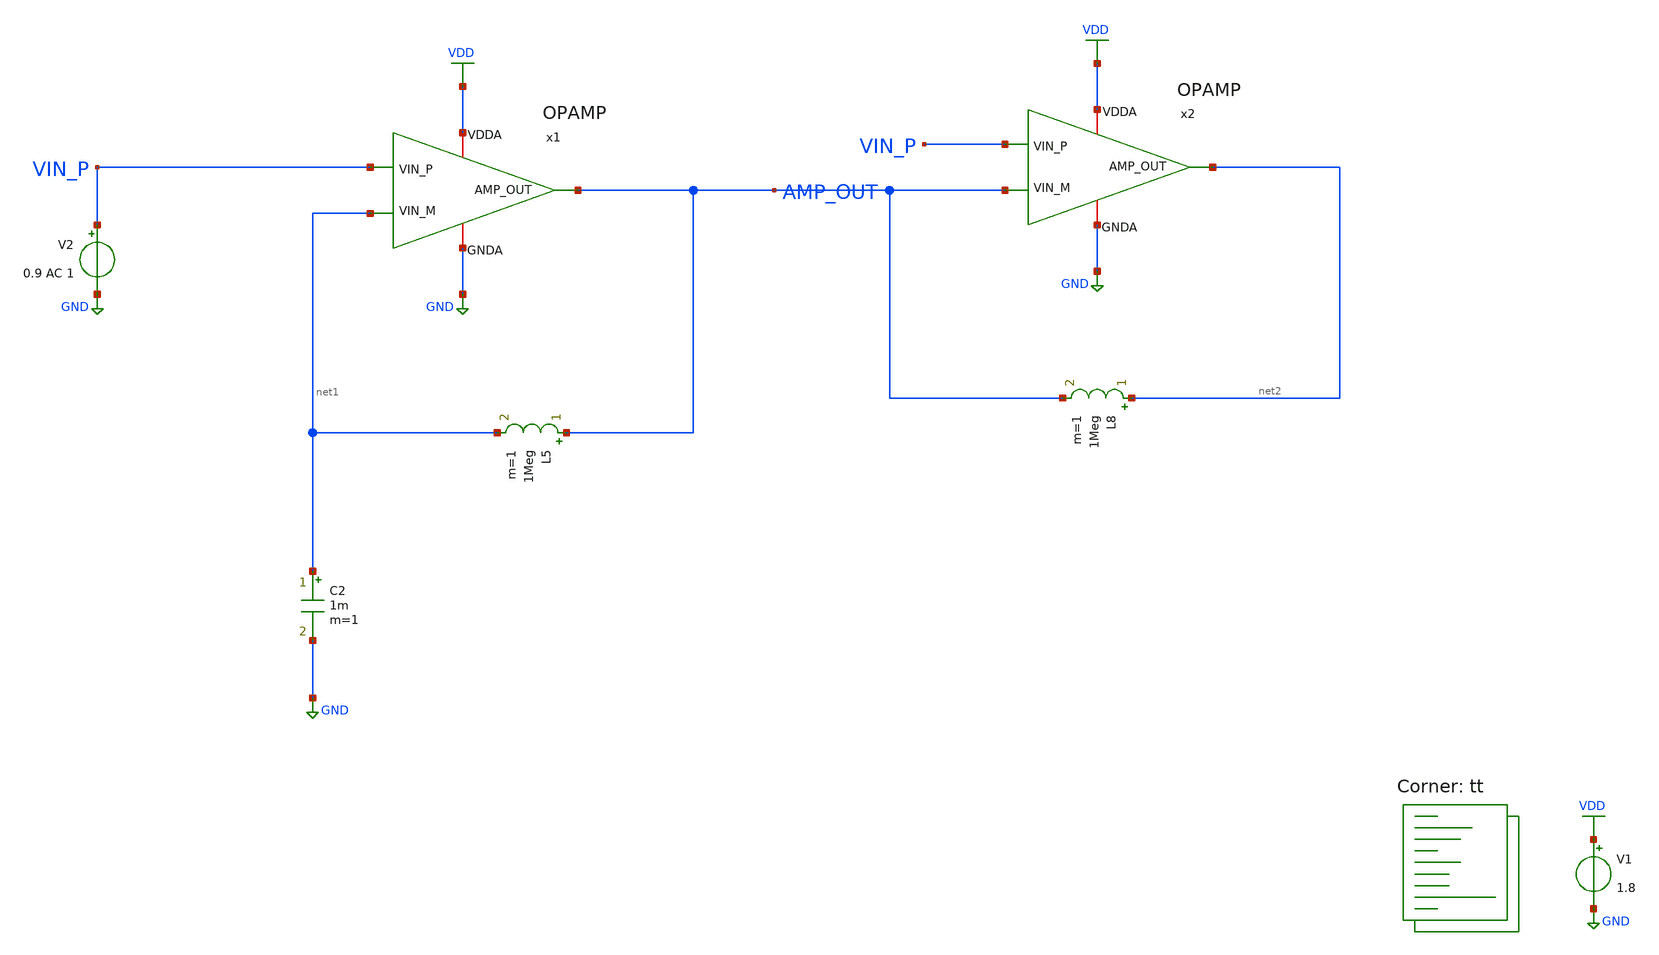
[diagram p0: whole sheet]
** sch_path: projects/ASU/EEE572/schematic/tb_OPAMP_CL.sch
**.subckt tb_OPAMP_CL
V1 VDD GND 1.8
V2 VIN_P GND 0.9 AC 1
C2 net1 GND 1m m=1
x1 VDD AMP_OUT VIN_P net1 GND OPAMP
L5 AMP_OUT net1 1Meg m=1
x2 VDD net2 VIN_P AMP_OUT GND OPAMP
L8 net2 AMP_OUT 1Meg m=1
**** begin user architecture code
.lib $::SKYWATER_MODELS/sky130.lib.spice tt



.options method=gear
.options wnflag=1
.options savecurrents

.save @m.xm34.msky130_fd_pr__nfet_01v8[gm] @m.xm34.msky130_fd_pr__nfet_01v8[vth] @m.xm35.msky130_fd_pr__nfet_01v8[gm] @m.xm35.msky130_fd_pr__nfet_01v8[vth] @m.xm36.msky130_fd_pr__nfet_01v8[gm] @m.xm36.msky130_fd_pr__nfet_01v8[vth] @m.xm37.msky130_fd_pr__nfet_01v8[gm] @m.xm37.msky130_fd_pr__nfet_01v8[vth] @m.xm44.msky130_fd_pr__nfet_01v8[gm] @m.xm44.msky130_fd_pr__nfet_01v8[vth] @m.xm38.msky130_fd_pr__nfet_01v8[gm] @m.xm38.msky130_fd_pr__nfet_01v8[vth] @m.xm39.msky130_fd_pr__nfet_01v8[gm] @m.xm39.msky130_fd_pr__nfet_01v8[vth] @m.xm43.msky130_fd_pr__pfet_01v8[gm] @m.xm43.msky130_fd_pr__pfet_01v8[vth] @m.xm42.msky130_fd_pr__pfet_01v8[gm] @m.xm42.msky130_fd_pr__pfet_01v8[vth] @m.xm46.msky130_fd_pr__pfet_01v8[gm] @m.xm46.msky130_fd_pr__pfet_01v8[vth] @m.xm41.msky130_fd_pr__pfet_01v8[gm] @m.xm41.msky130_fd_pr__pfet_01v8[vth] @m.xm40.msky130_fd_pr__pfet_01v8[gm] @m.xm40.msky130_fd_pr__pfet_01v8[vth] @m.xm45.msky130_fd_pr__pfet_01v8[gm] @m.xm45.msky130_fd_pr__pfet_01v8[vth] @m.xm29.msky130_fd_pr__pfet_01v8[gm] @m.xm29.msky130_fd_pr__pfet_01v8[vth] @m.xm30.msky130_fd_pr__pfet_01v8[gm] @m.xm30.msky130_fd_pr__pfet_01v8[vth] @m.xm31.msky130_fd_pr__nfet_01v8[gm] @m.xm31.msky130_fd_pr__nfet_01v8[vth] @m.xm32.msky130_fd_pr__nfet_01v8[gm] @m.xm32.msky130_fd_pr__nfet_01v8[vth] @m.xm15.msky130_fd_pr__pfet_01v8[gm] @m.xm15.msky130_fd_pr__pfet_01v8[vth] @m.xm14.msky130_fd_pr__pfet_01v8[gm] @m.xm14.msky130_fd_pr__pfet_01v8[vth] @m.xm17.msky130_fd_pr__pfet_01v8[gm] @m.xm17.msky130_fd_pr__pfet_01v8[vth] @m.xm16.msky130_fd_pr__pfet_01v8[gm] @m.xm16.msky130_fd_pr__pfet_01v8[vth] @m.xm27.msky130_fd_pr__nfet_01v8[gm] @m.xm27.msky130_fd_pr__nfet_01v8[vth] @m.xm28.msky130_fd_pr__nfet_01v8[gm] @m.xm28.msky130_fd_pr__nfet_01v8[vth] @m.xm19.msky130_fd_pr__nfet_01v8[gm] @m.xm19.msky130_fd_pr__nfet_01v8[vth] @m.xm20.msky130_fd_pr__nfet_01v8[gm] @m.xm20.msky130_fd_pr__nfet_01v8[vth] @m.xm21.msky130_fd_pr__nfet_01v8[gm] @m.xm21.msky130_fd_pr__nfet_01v8[vth] @m.xm33.msky130_fd_pr__pfet_01v8[gm] @m.xm33.msky130_fd_pr__pfet_01v8[vth] @m.xm22.msky130_fd_pr__nfet_01v8[gm] @m.xm22.msky130_fd_pr__nfet_01v8[vth] @m.xm26.msky130_fd_pr__nfet_01v8[gm] @m.xm26.msky130_fd_pr__nfet_01v8[vth] @m.xm24.msky130_fd_pr__nfet_01v8[gm] @m.xm24.msky130_fd_pr__nfet_01v8[vth] @m.xm18.msky130_fd_pr__nfet_01v8[gm] @m.xm18.msky130_fd_pr__nfet_01v8[vth]


.control

  let start_DC = 0.8
  let stop_DC = 1.2
  let index = 0.8
  dowhile start_DC <= stop_DC

    alter @V3[pulse] = [ 0 1.8 $&start_DC 1ns 1ns 24ns 50ns ]
    save v(amp_out) v(ph(amp_out))
    ac dec 20 1k 10G
    remzerovec
    echo $&start_DC
    write tb_OPAMP_OL_{$&index}.raw
    set appendwrite
    reset
    let index = index + 1
    let start_DC = start_DC + 0.1

  end

.endc




**** end user architecture code
**.ends

* expanding   symbol:  OPAMP.sym # of pins=5
** sym_path: projects/ASU/EEE572/schematic/OPAMP.sym
** sch_path: projects/ASU/EEE572/schematic/OPAMP.sch
.subckt OPAMP VDDA AMP_OUT VIN_P VIN_M GNDA
*.iopin GNDA
*.iopin VDDA
*.ipin VIN_P
*.ipin VIN_M
*.opin AMP_OUT
XM1 V_REF V_REF V_RES GND sky130_fd_pr__nfet_01v8 L=0.3 W=32 nf=8 ad='int((nf+1)/2) * W/nf * 0.29' as='int((nf+2)/2) * W/nf * 0.29'
+ pd='2*int((nf+1)/2) * (W/nf + 0.29)' ps='2*int((nf+2)/2) * (W/nf + 0.29)' nrd='0.29 / W' nrs='0.29 / W'
+ sa=0 sb=0 sd=0 mult=1 m=1
XM2 V_REF_MIR V_REF_MIR GNDA GNDA sky130_fd_pr__nfet_01v8 L=0.3 W=8 nf=2 ad='int((nf+1)/2) * W/nf * 0.29'
+ as='int((nf+2)/2) * W/nf * 0.29' pd='2*int((nf+1)/2) * (W/nf + 0.29)' ps='2*int((nf+2)/2) * (W/nf + 0.29)'
+ nrd='0.29 / W' nrs='0.29 / W' sa=0 sb=0 sd=0 mult=1 m=1
XM5 START_UP V_REF_MIR GNDA GNDA sky130_fd_pr__nfet_01v8 L=0.3 W=8 nf=2 ad='int((nf+1)/2) * W/nf * 0.29'
+ as='int((nf+2)/2) * W/nf * 0.29' pd='2*int((nf+1)/2) * (W/nf + 0.29)' ps='2*int((nf+2)/2) * (W/nf + 0.29)'
+ nrd='0.29 / W' nrs='0.29 / W' sa=0 sb=0 sd=0 mult=1 m=1
XM7 Vbiasp START_UP V_REF_MIR GNDA sky130_fd_pr__nfet_01v8 L=0.3 W=8 nf=2 ad='int((nf+1)/2) * W/nf * 0.29'
+ as='int((nf+2)/2) * W/nf * 0.29' pd='2*int((nf+1)/2) * (W/nf + 0.29)' ps='2*int((nf+2)/2) * (W/nf + 0.29)'
+ nrd='0.29 / W' nrs='0.29 / W' sa=0 sb=0 sd=0 mult=1 m=1
XM6 START_UP START_UP VDD VDD sky130_fd_pr__pfet_01v8 L=20 W=0.5 nf=1 ad='int((nf+1)/2) * W/nf * 0.29'
+ as='int((nf+2)/2) * W/nf * 0.29' pd='2*int((nf+1)/2) * (W/nf + 0.29)' ps='2*int((nf+2)/2) * (W/nf + 0.29)'
+ nrd='0.29 / W' nrs='0.29 / W' sa=0 sb=0 sd=0 mult=1 m=1
XM3 V_REF Vbiasp VDDA VDDA sky130_fd_pr__pfet_01v8 L=0.3 W=24 nf=6 ad='int((nf+1)/2) * W/nf * 0.29' as='int((nf+2)/2) * W/nf * 0.29'
+ pd='2*int((nf+1)/2) * (W/nf + 0.29)' ps='2*int((nf+2)/2) * (W/nf + 0.29)' nrd='0.29 / W' nrs='0.29 / W'
+ sa=0 sb=0 sd=0 mult=1 m=1
XM4 V_REF_MIR Vbiasp VDDA VDDA sky130_fd_pr__pfet_01v8 L=0.3 W=24 nf=6 ad='int((nf+1)/2) * W/nf * 0.29'
+ as='int((nf+2)/2) * W/nf * 0.29' pd='2*int((nf+1)/2) * (W/nf + 0.29)' ps='2*int((nf+2)/2) * (W/nf + 0.29)'
+ nrd='0.29 / W' nrs='0.29 / W' sa=0 sb=0 sd=0 mult=1 m=1
XM8 Vbiasp V_REF_MIR GNDA GNDA sky130_fd_pr__nfet_01v8 L=0.3 W=8 nf=2 ad='int((nf+1)/2) * W/nf * 0.29'
+ as='int((nf+2)/2) * W/nf * 0.29' pd='2*int((nf+1)/2) * (W/nf + 0.29)' ps='2*int((nf+2)/2) * (W/nf + 0.29)'
+ nrd='0.29 / W' nrs='0.29 / W' sa=0 sb=0 sd=0 mult=1 m=1
XM9 Vbiasp_MIR V_REF GNDA GNDA sky130_fd_pr__nfet_01v8 L=0.3 W=8 nf=2 ad='int((nf+1)/2) * W/nf * 0.29'
+ as='int((nf+2)/2) * W/nf * 0.29' pd='2*int((nf+1)/2) * (W/nf + 0.29)' ps='2*int((nf+2)/2) * (W/nf + 0.29)'
+ nrd='0.29 / W' nrs='0.29 / W' sa=0 sb=0 sd=0 mult=1 m=1
XM10 Vbiasp Vbiasp_MIR VDDA VDDA sky130_fd_pr__pfet_01v8 L=0.3 W=24 nf=6 ad='int((nf+1)/2) * W/nf * 0.29'
+ as='int((nf+2)/2) * W/nf * 0.29' pd='2*int((nf+1)/2) * (W/nf + 0.29)' ps='2*int((nf+2)/2) * (W/nf + 0.29)'
+ nrd='0.29 / W' nrs='0.29 / W' sa=0 sb=0 sd=0 mult=1 m=1
XM11 Vbiasp_MIR Vbiasp_MIR VDDA VDDA sky130_fd_pr__pfet_01v8 L=0.3 W=24 nf=6 ad='int((nf+1)/2) * W/nf * 0.29'
+ as='int((nf+2)/2) * W/nf * 0.29' pd='2*int((nf+1)/2) * (W/nf + 0.29)' ps='2*int((nf+2)/2) * (W/nf + 0.29)'
+ nrd='0.29 / W' nrs='0.29 / W' sa=0 sb=0 sd=0 mult=1 m=1
XM12 Vbias3 Vbias3 GNDA GNDA sky130_fd_pr__nfet_01v8 L=4 W=4 nf=1 ad='int((nf+1)/2) * W/nf * 0.29' as='int((nf+2)/2) * W/nf * 0.29'
+ pd='2*int((nf+1)/2) * (W/nf + 0.29)' ps='2*int((nf+2)/2) * (W/nf + 0.29)' nrd='0.29 / W' nrs='0.29 / W'
+ sa=0 sb=0 sd=0 mult=1 m=1
XM13 Vbias3 Vbiasp VDDA VDDA sky130_fd_pr__pfet_01v8 L=0.3 W=24 nf=6 ad='int((nf+1)/2) * W/nf * 0.29'
+ as='int((nf+2)/2) * W/nf * 0.29' pd='2*int((nf+1)/2) * (W/nf + 0.29)' ps='2*int((nf+2)/2) * (W/nf + 0.29)'
+ nrd='0.29 / W' nrs='0.29 / W' sa=0 sb=0 sd=0 mult=1 m=1
XM14 net1 Vbias1 VDDA VDDA sky130_fd_pr__pfet_01v8 L=0.3 W=24 nf=6 ad='int((nf+1)/2) * W/nf * 0.29' as='int((nf+2)/2) * W/nf * 0.29'
+ pd='2*int((nf+1)/2) * (W/nf + 0.29)' ps='2*int((nf+2)/2) * (W/nf + 0.29)' nrd='0.29 / W' nrs='0.29 / W'
+ sa=0 sb=0 sd=0 mult=1 m=1
XM15 Vhigh Vbias1 VDDA VDDA sky130_fd_pr__pfet_01v8 L=0.3 W=24 nf=6 ad='int((nf+1)/2) * W/nf * 0.29'
+ as='int((nf+2)/2) * W/nf * 0.29' pd='2*int((nf+1)/2) * (W/nf + 0.29)' ps='2*int((nf+2)/2) * (W/nf + 0.29)'
+ nrd='0.29 / W' nrs='0.29 / W' sa=0 sb=0 sd=0 mult=1 m=1
XM16 Vncas Vbias2 net1 VDDA sky130_fd_pr__pfet_01v8 L=0.3 W=24 nf=6 ad='int((nf+1)/2) * W/nf * 0.29'
+ as='int((nf+2)/2) * W/nf * 0.29' pd='2*int((nf+1)/2) * (W/nf + 0.29)' ps='2*int((nf+2)/2) * (W/nf + 0.29)'
+ nrd='0.29 / W' nrs='0.29 / W' sa=0 sb=0 sd=0 mult=1 m=1
XM17 Vbias1 Vbias2 Vhigh VDDA sky130_fd_pr__pfet_01v8 L=0.3 W=24 nf=6 ad='int((nf+1)/2) * W/nf * 0.29'
+ as='int((nf+2)/2) * W/nf * 0.29' pd='2*int((nf+1)/2) * (W/nf + 0.29)' ps='2*int((nf+2)/2) * (W/nf + 0.29)'
+ nrd='0.29 / W' nrs='0.29 / W' sa=0 sb=0 sd=0 mult=1 m=1
XM18 net2 Vbias4 GNDA GNDA sky130_fd_pr__nfet_01v8 L=0.3 W=8 nf=2 ad='int((nf+1)/2) * W/nf * 0.29' as='int((nf+2)/2) * W/nf * 0.29'
+ pd='2*int((nf+1)/2) * (W/nf + 0.29)' ps='2*int((nf+2)/2) * (W/nf + 0.29)' nrd='0.29 / W' nrs='0.29 / W'
+ sa=0 sb=0 sd=0 mult=1 m=1
XM19 Vncas Vncas Vncas_btw GNDA sky130_fd_pr__nfet_01v8 L=0.3 W=4 nf=2 ad='int((nf+1)/2) * W/nf * 0.29'
+ as='int((nf+2)/2) * W/nf * 0.29' pd='2*int((nf+1)/2) * (W/nf + 0.29)' ps='2*int((nf+2)/2) * (W/nf + 0.29)'
+ nrd='0.29 / W' nrs='0.29 / W' sa=0 sb=0 sd=0 mult=1 m=1
XM20 Vncas_btw Vbias3 net3 GNDA sky130_fd_pr__nfet_01v8 L=0.3 W=4 nf=2 ad='int((nf+1)/2) * W/nf * 0.29'
+ as='int((nf+2)/2) * W/nf * 0.29' pd='2*int((nf+1)/2) * (W/nf + 0.29)' ps='2*int((nf+2)/2) * (W/nf + 0.29)'
+ nrd='0.29 / W' nrs='0.29 / W' sa=0 sb=0 sd=0 mult=1 m=1
XM21 net3 Vncas_btw GNDA GNDA sky130_fd_pr__nfet_01v8 L=0.3 W=4 nf=2 ad='int((nf+1)/2) * W/nf * 0.29'
+ as='int((nf+2)/2) * W/nf * 0.29' pd='2*int((nf+1)/2) * (W/nf + 0.29)' ps='2*int((nf+2)/2) * (W/nf + 0.29)'
+ nrd='0.29 / W' nrs='0.29 / W' sa=0 sb=0 sd=0 mult=1 m=1
XM25 Vbias4 Vbiasp VDDA VDDA sky130_fd_pr__pfet_01v8 L=0.3 W=24 nf=6 ad='int((nf+1)/2) * W/nf * 0.29'
+ as='int((nf+2)/2) * W/nf * 0.29' pd='2*int((nf+1)/2) * (W/nf + 0.29)' ps='2*int((nf+2)/2) * (W/nf + 0.29)'
+ nrd='0.29 / W' nrs='0.29 / W' sa=0 sb=0 sd=0 mult=1 m=1
XM27 Vbias4 Vbias3 Vlow GNDA sky130_fd_pr__nfet_01v8 L=0.3 W=8 nf=2 ad='int((nf+1)/2) * W/nf * 0.29'
+ as='int((nf+2)/2) * W/nf * 0.29' pd='2*int((nf+1)/2) * (W/nf + 0.29)' ps='2*int((nf+2)/2) * (W/nf + 0.29)'
+ nrd='0.29 / W' nrs='0.29 / W' sa=0 sb=0 sd=0 mult=1 m=1
XM28 Vlow Vbias4 GNDA GNDA sky130_fd_pr__nfet_01v8 L=0.3 W=8 nf=2 ad='int((nf+1)/2) * W/nf * 0.29' as='int((nf+2)/2) * W/nf * 0.29'
+ pd='2*int((nf+1)/2) * (W/nf + 0.29)' ps='2*int((nf+2)/2) * (W/nf + 0.29)' nrd='0.29 / W' nrs='0.29 / W'
+ sa=0 sb=0 sd=0 mult=1 m=1
XM29 Vds2 Vgs2 VDDA VDDA sky130_fd_pr__pfet_01v8 L=0.15 W=12 nf=6 ad='int((nf+1)/2) * W/nf * 0.29' as='int((nf+2)/2) * W/nf * 0.29'
+ pd='2*int((nf+1)/2) * (W/nf + 0.29)' ps='2*int((nf+2)/2) * (W/nf + 0.29)' nrd='0.29 / W' nrs='0.29 / W'
+ sa=0 sb=0 sd=0 mult=1 m=1
XM30 Vgs2 Vbias2 Vds2 VDDA sky130_fd_pr__pfet_01v8 L=0.15 W=12 nf=6 ad='int((nf+1)/2) * W/nf * 0.29'
+ as='int((nf+2)/2) * W/nf * 0.29' pd='2*int((nf+1)/2) * (W/nf + 0.29)' ps='2*int((nf+2)/2) * (W/nf + 0.29)'
+ nrd='0.29 / W' nrs='0.29 / W' sa=0 sb=0 sd=0 mult=1 m=1
XM31 Vpcas Vbias3 Vds3 GNDA sky130_fd_pr__nfet_01v8 L=0.3 W=8 nf=2 ad='int((nf+1)/2) * W/nf * 0.29' as='int((nf+2)/2) * W/nf * 0.29'
+ pd='2*int((nf+1)/2) * (W/nf + 0.29)' ps='2*int((nf+2)/2) * (W/nf + 0.29)' nrd='0.29 / W' nrs='0.29 / W'
+ sa=0 sb=0 sd=0 mult=1 m=1
XM32 Vds3 Vbias4 GNDA GNDA sky130_fd_pr__nfet_01v8 L=0.3 W=8 nf=2 ad='int((nf+1)/2) * W/nf * 0.29' as='int((nf+2)/2) * W/nf * 0.29'
+ pd='2*int((nf+1)/2) * (W/nf + 0.29)' ps='2*int((nf+2)/2) * (W/nf + 0.29)' nrd='0.29 / W' nrs='0.29 / W'
+ sa=0 sb=0 sd=0 mult=1 m=1
XM33 Vpcas Vpcas Vgs2 VDDA sky130_fd_pr__pfet_01v8 L=0.15 W=12 nf=1 ad='int((nf+1)/2) * W/nf * 0.29'
+ as='int((nf+2)/2) * W/nf * 0.29' pd='2*int((nf+1)/2) * (W/nf + 0.29)' ps='2*int((nf+2)/2) * (W/nf + 0.29)'
+ nrd='0.29 / W' nrs='0.29 / W' sa=0 sb=0 sd=0 mult=1 m=1
XM22 Vbias1 Vbias3 net2 GNDA sky130_fd_pr__nfet_01v8 L=0.3 W=8 nf=2 ad='int((nf+1)/2) * W/nf * 0.29'
+ as='int((nf+2)/2) * W/nf * 0.29' pd='2*int((nf+1)/2) * (W/nf + 0.29)' ps='2*int((nf+2)/2) * (W/nf + 0.29)'
+ nrd='0.29 / W' nrs='0.29 / W' sa=0 sb=0 sd=0 mult=1 m=1
XM23 Vbias2 Vbias2 VDDA VDDA sky130_fd_pr__pfet_01v8 L=1.5 W=24 nf=1 ad='int((nf+1)/2) * W/nf * 0.29'
+ as='int((nf+2)/2) * W/nf * 0.29' pd='2*int((nf+1)/2) * (W/nf + 0.29)' ps='2*int((nf+2)/2) * (W/nf + 0.29)'
+ nrd='0.29 / W' nrs='0.29 / W' sa=0 sb=0 sd=0 mult=1 m=1
XM24 net4 Vbias4 GNDA GNDA sky130_fd_pr__nfet_01v8 L=0.3 W=8 nf=2 ad='int((nf+1)/2) * W/nf * 0.29' as='int((nf+2)/2) * W/nf * 0.29'
+ pd='2*int((nf+1)/2) * (W/nf + 0.29)' ps='2*int((nf+2)/2) * (W/nf + 0.29)' nrd='0.29 / W' nrs='0.29 / W'
+ sa=0 sb=0 sd=0 mult=1 m=1
XM26 Vbias2 Vbias3 net4 GNDA sky130_fd_pr__nfet_01v8 L=0.3 W=8 nf=2 ad='int((nf+1)/2) * W/nf * 0.29'
+ as='int((nf+2)/2) * W/nf * 0.29' pd='2*int((nf+1)/2) * (W/nf + 0.29)' ps='2*int((nf+2)/2) * (W/nf + 0.29)'
+ nrd='0.29 / W' nrs='0.29 / W' sa=0 sb=0 sd=0 mult=1 m=1
XC1 Vbiasp VDDA sky130_fd_pr__cap_mim_m3_1 W=2 L=2 MF=4 m=4
XM34 V_tail_btw Vbias4 GNDA GNDA sky130_fd_pr__nfet_01v8 L=0.3 W=32 nf=5 ad='int((nf+1)/2) * W/nf * 0.29'
+ as='int((nf+2)/2) * W/nf * 0.29' pd='2*int((nf+1)/2) * (W/nf + 0.29)' ps='2*int((nf+2)/2) * (W/nf + 0.29)'
+ nrd='0.29 / W' nrs='0.29 / W' sa=0 sb=0 sd=0 mult=1 m=1
XM35 Vp Vbias3 V_tail_btw GNDA sky130_fd_pr__nfet_01v8 L=0.3 W=32 nf=5 ad='int((nf+1)/2) * W/nf * 0.29'
+ as='int((nf+2)/2) * W/nf * 0.29' pd='2*int((nf+1)/2) * (W/nf + 0.29)' ps='2*int((nf+2)/2) * (W/nf + 0.29)'
+ nrd='0.29 / W' nrs='0.29 / W' sa=0 sb=0 sd=0 mult=1 m=1
XM36 Vd1 VIN_P Vp GNDA sky130_fd_pr__nfet_01v8 L=0.15 W=24 nf=2 ad='int((nf+1)/2) * W/nf * 0.29' as='int((nf+2)/2) * W/nf * 0.29'
+ pd='2*int((nf+1)/2) * (W/nf + 0.29)' ps='2*int((nf+2)/2) * (W/nf + 0.29)' nrd='0.29 / W' nrs='0.29 / W'
+ sa=0 sb=0 sd=0 mult=1 m=1
XM37 Vd2 VIN_M Vp GNDA sky130_fd_pr__nfet_01v8 L=0.15 W=24 nf=2 ad='int((nf+1)/2) * W/nf * 0.29' as='int((nf+2)/2) * W/nf * 0.29'
+ pd='2*int((nf+1)/2) * (W/nf + 0.29)' ps='2*int((nf+2)/2) * (W/nf + 0.29)' nrd='0.29 / W' nrs='0.29 / W'
+ sa=0 sb=0 sd=0 mult=1 m=1
XM38 AMP_MIR Vb1 Vd1 GND sky130_fd_pr__nfet_01v8 L=0.15 W=24 nf=2 ad='int((nf+1)/2) * W/nf * 0.29' as='int((nf+2)/2) * W/nf * 0.29'
+ pd='2*int((nf+1)/2) * (W/nf + 0.29)' ps='2*int((nf+2)/2) * (W/nf + 0.29)' nrd='0.29 / W' nrs='0.29 / W'
+ sa=0 sb=0 sd=0 mult=1 m=1
XM39 AMP_OUT Vb1 Vd2 GND sky130_fd_pr__nfet_01v8 L=0.15 W=24 nf=2 ad='int((nf+1)/2) * W/nf * 0.29' as='int((nf+2)/2) * W/nf * 0.29'
+ pd='2*int((nf+1)/2) * (W/nf + 0.29)' ps='2*int((nf+2)/2) * (W/nf + 0.29)' nrd='0.29 / W' nrs='0.29 / W'
+ sa=0 sb=0 sd=0 mult=1 m=1
XM40 net6 AMP_MIR VDDA VDDA sky130_fd_pr__pfet_01v8 L=0.15 W=72 nf=6 ad='int((nf+1)/2) * W/nf * 0.29'
+ as='int((nf+2)/2) * W/nf * 0.29' pd='2*int((nf+1)/2) * (W/nf + 0.29)' ps='2*int((nf+2)/2) * (W/nf + 0.29)'
+ nrd='0.29 / W' nrs='0.29 / W' sa=0 sb=0 sd=0 mult=1 m=1
XM41 net5 AMP_MIR VDDA VDDA sky130_fd_pr__pfet_01v8 L=0.15 W=72 nf=6 ad='int((nf+1)/2) * W/nf * 0.29'
+ as='int((nf+2)/2) * W/nf * 0.29' pd='2*int((nf+1)/2) * (W/nf + 0.29)' ps='2*int((nf+2)/2) * (W/nf + 0.29)'
+ nrd='0.29 / W' nrs='0.29 / W' sa=0 sb=0 sd=0 mult=1 m=1
XM42 AMP_OUT Vbias2 net6 VDDA sky130_fd_pr__pfet_01v8 L=0.15 W=72 nf=6 ad='int((nf+1)/2) * W/nf * 0.29'
+ as='int((nf+2)/2) * W/nf * 0.29' pd='2*int((nf+1)/2) * (W/nf + 0.29)' ps='2*int((nf+2)/2) * (W/nf + 0.29)'
+ nrd='0.29 / W' nrs='0.29 / W' sa=0 sb=0 sd=0 mult=1 m=1
XM43 AMP_MIR Vbias2 net5 VDDA sky130_fd_pr__pfet_01v8 L=0.15 W=72 nf=6 ad='int((nf+1)/2) * W/nf * 0.29'
+ as='int((nf+2)/2) * W/nf * 0.29' pd='2*int((nf+1)/2) * (W/nf + 0.29)' ps='2*int((nf+2)/2) * (W/nf + 0.29)'
+ nrd='0.29 / W' nrs='0.29 / W' sa=0 sb=0 sd=0 mult=1 m=1
XM44 Vb1 Vb1 Vp GNDA sky130_fd_pr__nfet_01v8 L=0.6 W=4 nf=1 ad='int((nf+1)/2) * W/nf * 0.29' as='int((nf+2)/2) * W/nf * 0.29'
+ pd='2*int((nf+1)/2) * (W/nf + 0.29)' ps='2*int((nf+2)/2) * (W/nf + 0.29)' nrd='0.29 / W' nrs='0.29 / W'
+ sa=0 sb=0 sd=0 mult=1 m=1
XM45 net7 Vbias1 VDDA VDDA sky130_fd_pr__pfet_01v8 L=0.3 W=24 nf=6 ad='int((nf+1)/2) * W/nf * 0.29' as='int((nf+2)/2) * W/nf * 0.29'
+ pd='2*int((nf+1)/2) * (W/nf + 0.29)' ps='2*int((nf+2)/2) * (W/nf + 0.29)' nrd='0.29 / W' nrs='0.29 / W'
+ sa=0 sb=0 sd=0 mult=1 m=1
XM46 Vb1 Vbias2 net7 VDDA sky130_fd_pr__pfet_01v8 L=0.3 W=24 nf=6 ad='int((nf+1)/2) * W/nf * 0.29' as='int((nf+2)/2) * W/nf * 0.29'
+ pd='2*int((nf+1)/2) * (W/nf + 0.29)' ps='2*int((nf+2)/2) * (W/nf + 0.29)' nrd='0.29 / W' nrs='0.29 / W'
+ sa=0 sb=0 sd=0 mult=1 m=1
XR1 GNDA V_RES GNDA sky130_fd_pr__res_high_po_0p35 L=8 mult=1 m=1
.ends

.GLOBAL GND
.GLOBAL VDD
.end
